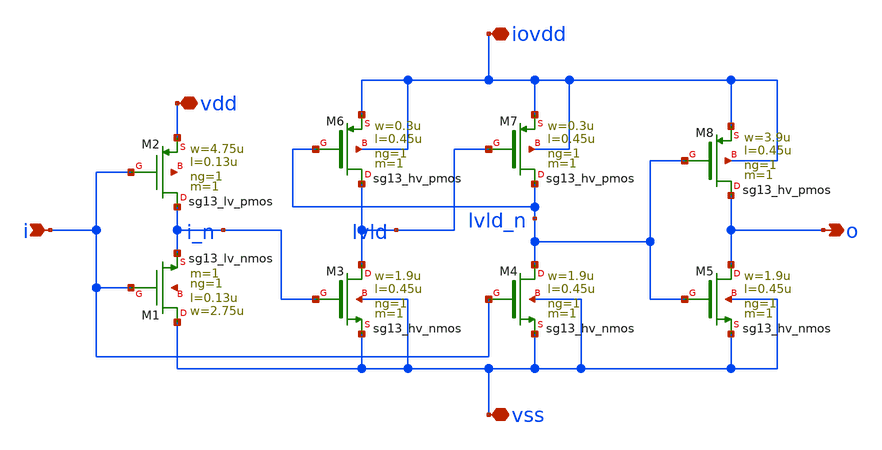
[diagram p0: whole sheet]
** sch_path: ihp-sg13g2/libs.ref/sg13g2_io/xschem/sg13g2_LevelUp.sch
**.subckt sg13g2_LevelUp vss iovdd vdd i o
*.iopin vss
*.iopin iovdd
*.iopin vdd
*.ipin i
*.opin o
XM1 vss i i_n net1 sg13_lv_nmos w=2.75u l=0.13u ng=1 m=1 mm_ok=1
XM2 i_n i vdd net2 sg13_lv_pmos w=4.75u l=0.13u ng=1 m=1 mm_ok=1
XM3 lvld i_n vss vss sg13_hv_nmos w=1.9u l=0.45u ng=1 m=1 mm_ok=1
XM4 lvld_n i vss vss sg13_hv_nmos w=1.9u l=0.45u ng=1 m=1 mm_ok=1
XM5 o lvld_n vss vss sg13_hv_nmos w=1.9u l=0.45u ng=1 m=1 mm_ok=1
XM6 lvld lvld_n iovdd iovdd sg13_hv_pmos w=0.3u l=0.45u ng=1 m=1 mm_ok=1
XM7 lvld_n lvld iovdd iovdd sg13_hv_pmos w=0.3u l=0.45u ng=1 m=1 mm_ok=1
XM8 o lvld_n iovdd iovdd sg13_hv_pmos w=3.9u l=0.45u ng=1 m=1 mm_ok=1
**.ends
.end
